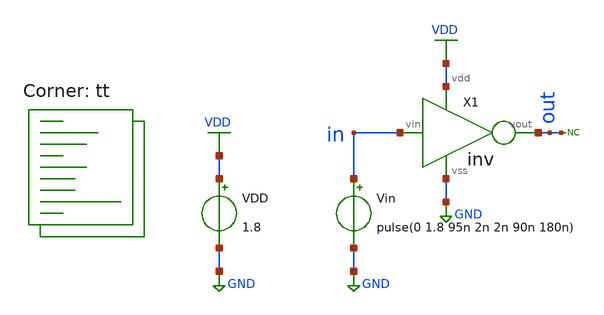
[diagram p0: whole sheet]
** sch_path: xsch/tb/inv/tb_inv_tran.sch
**.subckt tb_inv_tran
Vin in GND pulse(0 1.8 95n 2n 2n 90n 180n)
VDD VDD GND 1.8
* noconn out
X1 in out VDD GND inv
**** begin user architecture code



.include ~/ttsky25b_tiny_chaos/mag/inv_extracted_files/inv_extracted.spice

* control language script

.control
tran 100p 500n               ; simulation command 1

set xbrushwidth=2
plot v(in) v(out)

write $inputdir/outtran.out v(in) v(out)

reset

dc vin 0 2 0.01              ; simulation command 2

plot v(out) v(out2) v(out3)               ; v(in) not required because it is the x axis already

write $inputdir/outdc.out v(out)

.endc
.end



.lib $::SKYWATER_MODELS/sky130.lib.spice tt
**** end user architecture code
**.ends

* expanding   symbol:  /home/bmott/ttsky25b_tiny_chaos/xsch/ip/logic/inv/inv.sym # of pins=4
** sym_path: xsch/ip/logic/inv/inv.sym
** sch_path: xsch/ip/logic/inv/inv.sch
.subckt inv vin vout vdd vss
*.ipin vin
*.opin vout
*.ipin vdd
*.ipin vss
XMn vout vin vss vss sky130_fd_pr__nfet_01v8 L=0.15 W=1 nf=1 ad='int((1 + 1)/2) * 1 / 1 * 0.29' as='int((1 + 2)/2) * 1 / 1 * 0.29'
+ pd='2*int((1 + 1)/2) * (1 / 1 + 0.29)' ps='2*int((1 + 2)/2) * (1 / 1 + 0.29)' nrd='0.29 / 1 ' nrs='0.29 / 1 '
+ sa=0 sb=0 sd=0 mult=1 m=1
XMp vout vin vdd vdd sky130_fd_pr__pfet_01v8 L=0.15 W=2 nf=1 ad='int((nf+1)/2) * W/nf * 0.29' as='int((nf+2)/2) * W/nf * 0.29'
+ pd='2*int((nf+1)/2) * (W/nf + 0.29)' ps='2*int((nf+2)/2) * (W/nf + 0.29)' nrd='0.29 / W' nrs='0.29 / W'
+ sa=0 sb=0 sd=0 mult=1 m=1
.ends

.GLOBAL VDD
.GLOBAL GND
.end
